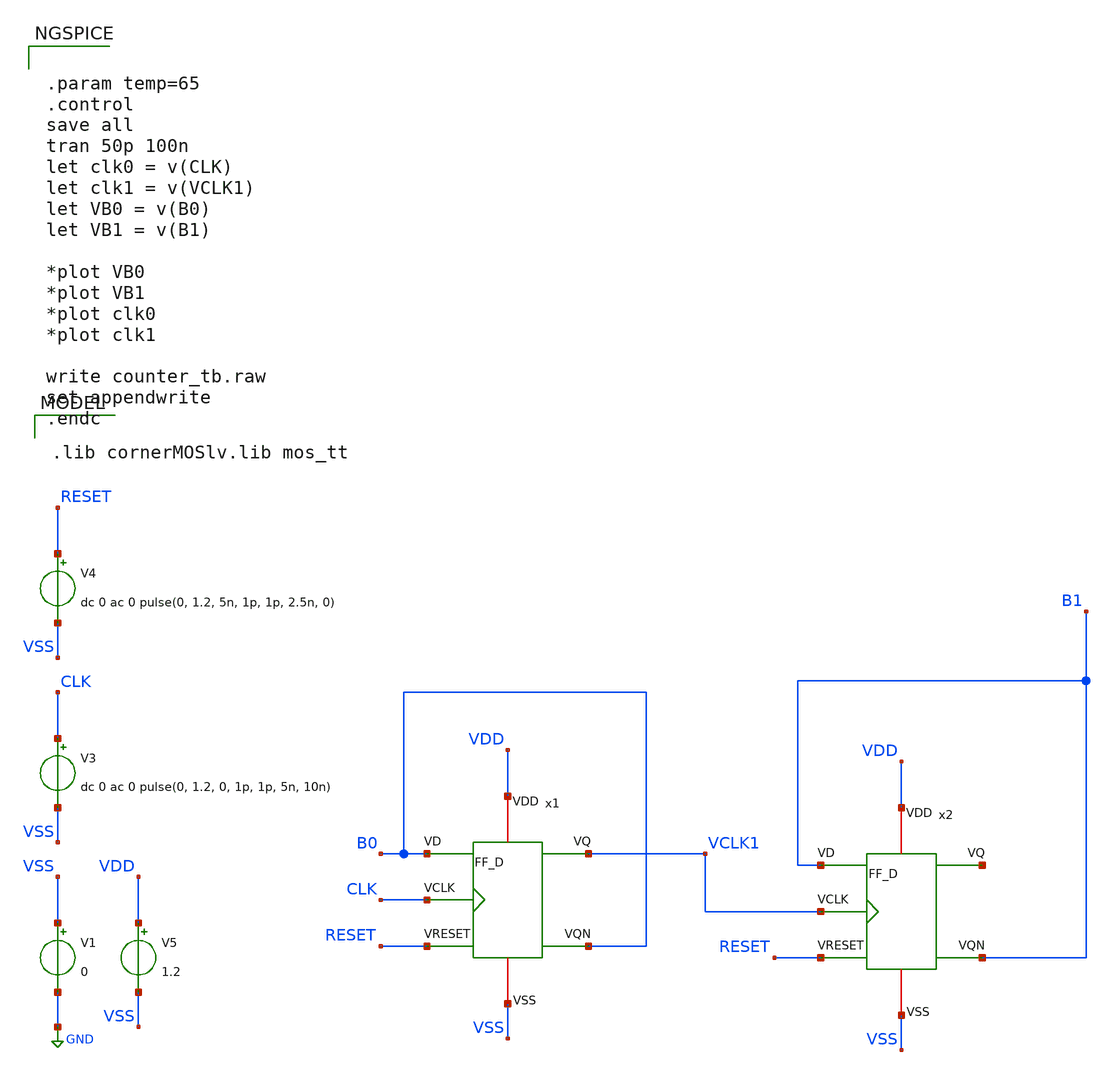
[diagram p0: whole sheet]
** sch_path: ADC8711-main/testbenches/tran/xschem/counter_tb.sch
**.subckt counter_tb
x1 VDD CLK RESET VSS VCLK1 B0 B0 FF_D
V1 VSS GND 0
V3 CLK VSS dc 0 ac 0 pulse(0, 1.2, 0, 1p, 1p, 5n, 10n)
V5 VDD VSS 1.2
x2 VDD VCLK1 RESET VSS net1 B1 B1 FF_D
V4 RESET VSS dc 0 ac 0 pulse(0, 1.2, 5n, 1p, 1p, 2.5n, 0)
**** begin user architecture code


.param temp=65
.control
save all
tran 50p 100n
let clk0 = v(CLK)
let clk1 = v(VCLK1)
let VB0 = v(B0)
let VB1 = v(B1)

*plot VB0
*plot VB1
*plot clk0
*plot clk1

write counter_tb.raw
set appendwrite
.endc



.lib cornerMOSlv.lib mos_tt

**** end user architecture code
**.ends
.GLOBAL GND
.end
